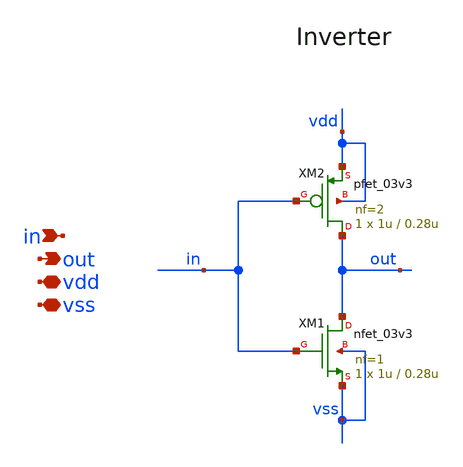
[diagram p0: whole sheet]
** sch_path: designs/DESIGN/DACFUTURE_EDU/inv/inv.sch
**.subckt inv in out vdd vss
*.ipin in
*.opin out
*.iopin vdd
*.iopin vss
XM1 out in vss vss nfet_03v3 L=0.28u W=1u nf=1 ad='int((nf+1)/2) * W/nf * 0.18u' as='int((nf+2)/2) * W/nf * 0.18u'
+ pd='2*int((nf+1)/2) * (W/nf + 0.18u)' ps='2*int((nf+2)/2) * (W/nf + 0.18u)' nrd='0.18u / W' nrs='0.18u / W'
+ sa=0 sb=0 sd=0 m=1
XM2 out in vdd vdd pfet_03v3 L=0.28u W=1u nf=2 ad='int((nf+1)/2) * W/nf * 0.18u' as='int((nf+2)/2) * W/nf * 0.18u'
+ pd='2*int((nf+1)/2) * (W/nf + 0.18u)' ps='2*int((nf+2)/2) * (W/nf + 0.18u)' nrd='0.18u / W' nrs='0.18u / W'
+ sa=0 sb=0 sd=0 m=1
**.ends
.end
